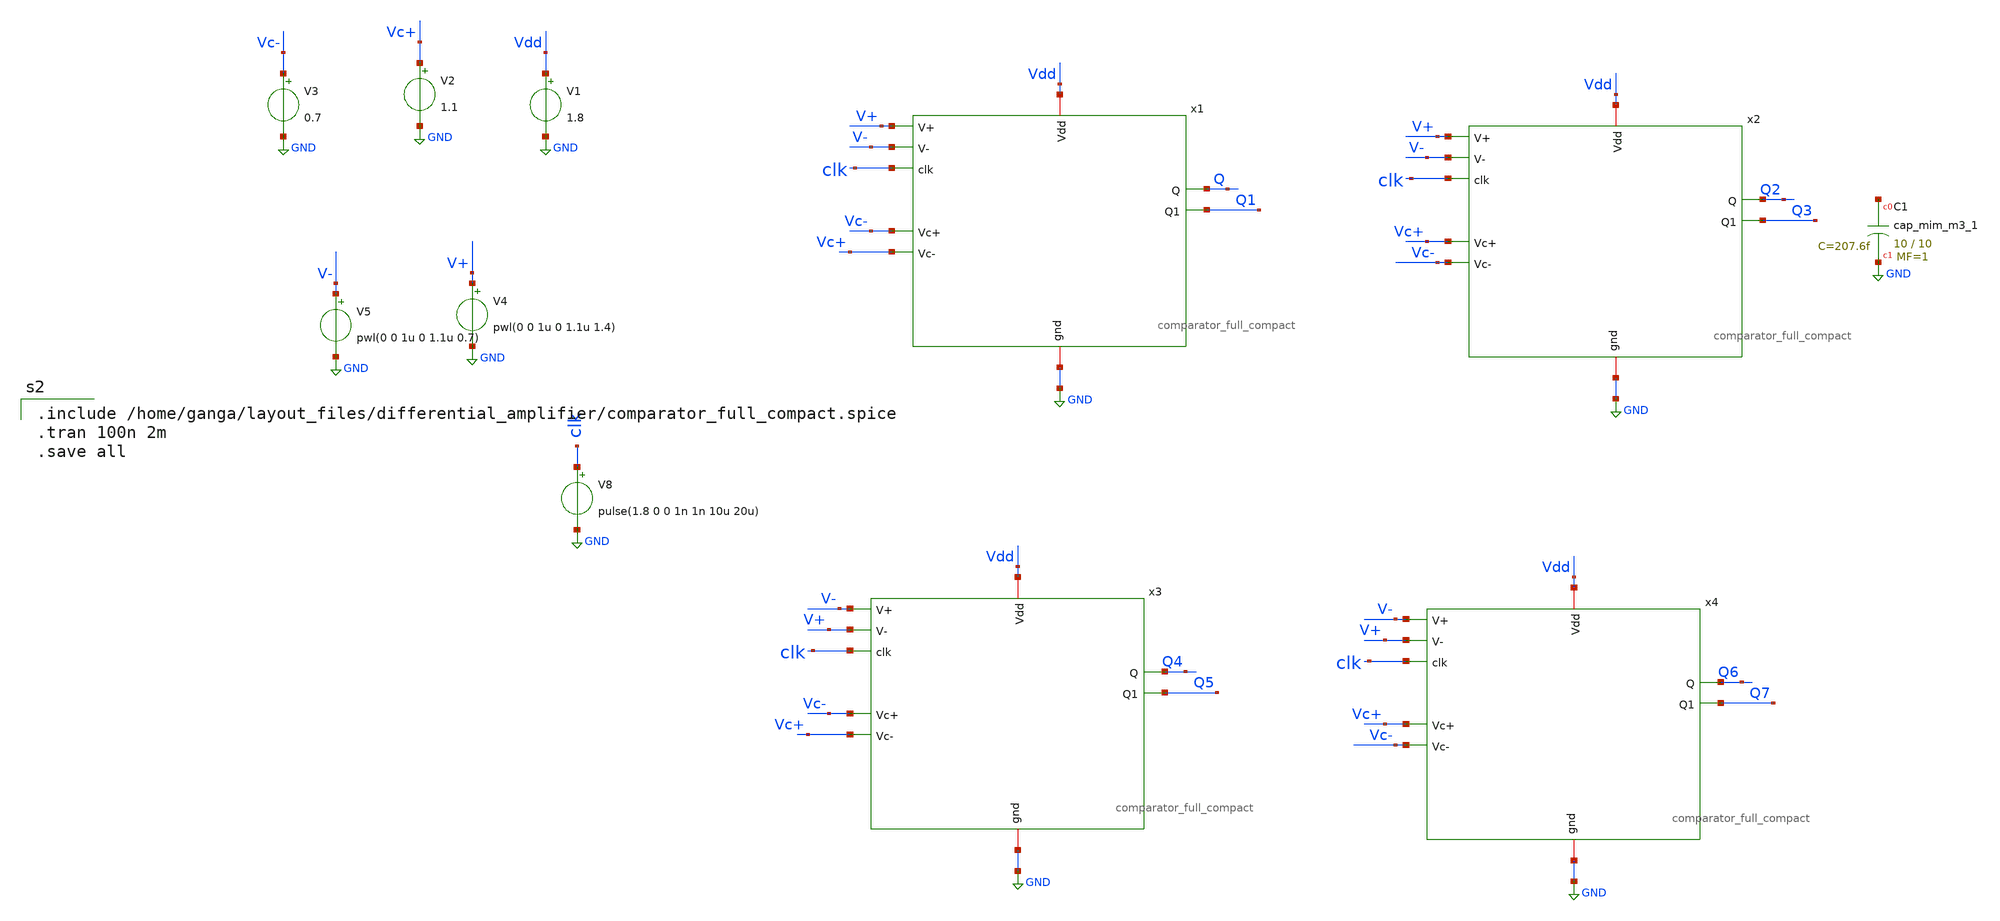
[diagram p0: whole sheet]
** sch_path: xschem/xschemfiles/comparator_test.sch
**.subckt comparator_test
V1 Vdd GND 1.8
V2 Vc+ GND 1.1
V3 Vc- GND 0.7
V4 V+ GND pwl(0 0 1u 0 1.1u 1.4)
V5 V- GND pwl(0 0 1u 0 1.1u 0.7)
V8 clk GND pulse(1.8 0 0 1n 1n 10u 20u)
x1 Vdd GND clk Vc+ V+ V- Vc- Q Q1 comparator_full_compact
x2 Vdd GND clk Vc- V+ V- Vc+ Q2 Q3 comparator_full_compact
XC1 net1 GND sky130_fd_pr__cap_mim_m3_1 W=10 L=10 MF=1 m=1
x3 Vdd GND clk Vc+ V- V+ Vc- Q4 Q5 comparator_full_compact
x4 Vdd GND clk Vc- V- V+ Vc+ Q6 Q7 comparator_full_compact
**** begin user architecture code

** opencircuitdesign pdks install
.lib $::SKYWATER_MODELS/sky130.lib.spice tt



.include /home/ganga/layout_files/differential_amplifier/comparator_full_compact.spice
.tran 100n 2m
.save all

**** end user architecture code
**.ends
.GLOBAL GND
.end
